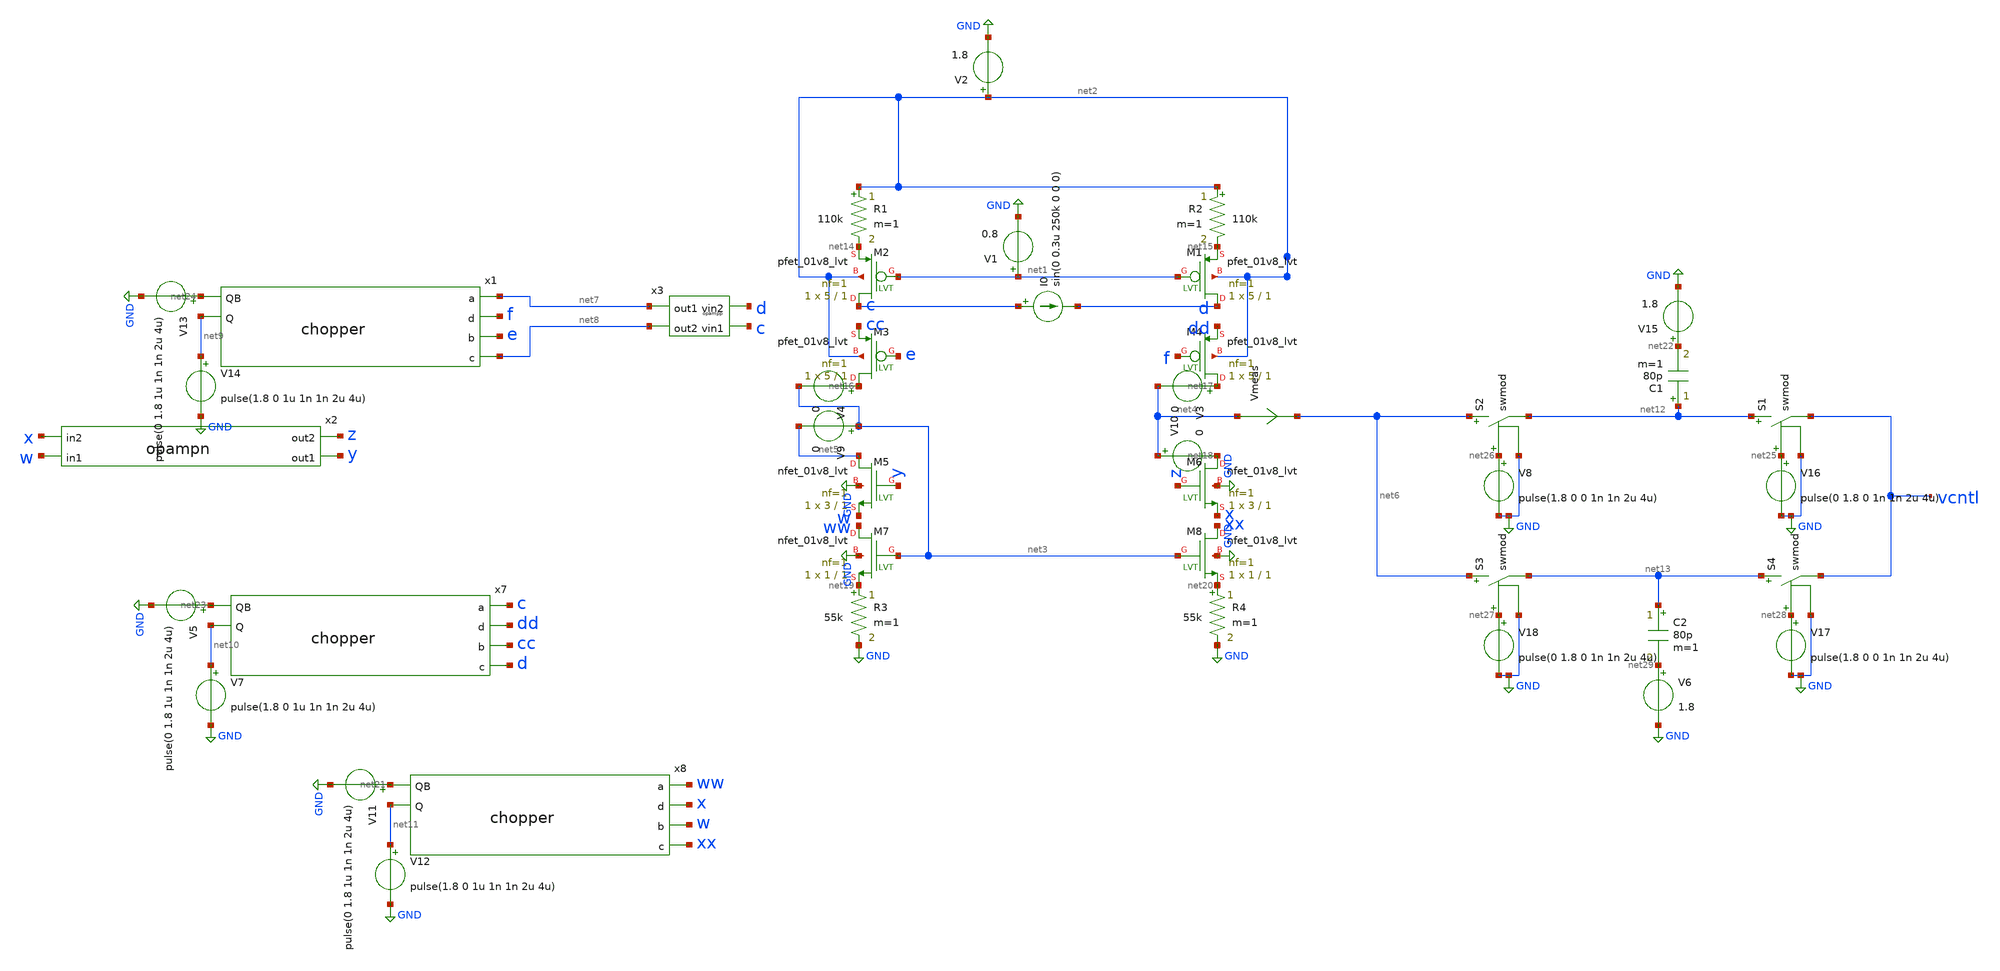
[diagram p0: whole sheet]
** sch_path: currentbuffer.sch
**.subckt currentbuffer
XM2 c net1 net14 net2 sky130_fd_pr__pfet_01v8_lvt L=1 W=5 nf=1 ad='int((nf+1)/2) * W/nf * 0.29' as='int((nf+2)/2) * W/nf * 0.29'
+ pd='2*int((nf+1)/2) * (W/nf + 0.29)' ps='2*int((nf+2)/2) * (W/nf + 0.29)' nrd='0.29 / W' nrs='0.29 / W'
+ sa=0 sb=0 sd=0 mult=1 m=1
R1 net2 net14 110k m=1
XM1 d net1 net15 net2 sky130_fd_pr__pfet_01v8_lvt L=1 W=5 nf=1 ad='int((nf+1)/2) * W/nf * 0.29' as='int((nf+2)/2) * W/nf * 0.29'
+ pd='2*int((nf+1)/2) * (W/nf + 0.29)' ps='2*int((nf+2)/2) * (W/nf + 0.29)' nrd='0.29 / W' nrs='0.29 / W'
+ sa=0 sb=0 sd=0 mult=1 m=1
R2 net2 net15 110k m=1
V1 net1 GND 0.8
XM3 net16 e cc net2 sky130_fd_pr__pfet_01v8_lvt L=1 W=5 nf=1 ad='int((nf+1)/2) * W/nf * 0.29' as='int((nf+2)/2) * W/nf * 0.29'
+ pd='2*int((nf+1)/2) * (W/nf + 0.29)' ps='2*int((nf+2)/2) * (W/nf + 0.29)' nrd='0.29 / W' nrs='0.29 / W'
+ sa=0 sb=0 sd=0 mult=1 m=1
XM4 net17 f dd net2 sky130_fd_pr__pfet_01v8_lvt L=1 W=5 nf=1 ad='int((nf+1)/2) * W/nf * 0.29' as='int((nf+2)/2) * W/nf * 0.29'
+ pd='2*int((nf+1)/2) * (W/nf + 0.29)' ps='2*int((nf+2)/2) * (W/nf + 0.29)' nrd='0.29 / W' nrs='0.29 / W'
+ sa=0 sb=0 sd=0 mult=1 m=1
XM5 net5 y w GND sky130_fd_pr__nfet_01v8_lvt L=1 W=3 nf=1 ad='int((nf+1)/2) * W/nf * 0.29' as='int((nf+2)/2) * W/nf * 0.29'
+ pd='2*int((nf+1)/2) * (W/nf + 0.29)' ps='2*int((nf+2)/2) * (W/nf + 0.29)' nrd='0.29 / W' nrs='0.29 / W'
+ sa=0 sb=0 sd=0 mult=1 m=1
XM6 net18 z x GND sky130_fd_pr__nfet_01v8_lvt L=1 W=3 nf=1 ad='int((nf+1)/2) * W/nf * 0.29' as='int((nf+2)/2) * W/nf * 0.29'
+ pd='2*int((nf+1)/2) * (W/nf + 0.29)' ps='2*int((nf+2)/2) * (W/nf + 0.29)' nrd='0.29 / W' nrs='0.29 / W'
+ sa=0 sb=0 sd=0 mult=1 m=1
XM7 ww net3 net19 GND sky130_fd_pr__nfet_01v8_lvt L=1 W=1 nf=1 ad='int((nf+1)/2) * W/nf * 0.29' as='int((nf+2)/2) * W/nf * 0.29'
+ pd='2*int((nf+1)/2) * (W/nf + 0.29)' ps='2*int((nf+2)/2) * (W/nf + 0.29)' nrd='0.29 / W' nrs='0.29 / W'
+ sa=0 sb=0 sd=0 mult=1 m=1
XM8 xx net3 net20 GND sky130_fd_pr__nfet_01v8_lvt L=1 W=1 nf=1 ad='int((nf+1)/2) * W/nf * 0.29' as='int((nf+2)/2) * W/nf * 0.29'
+ pd='2*int((nf+1)/2) * (W/nf + 0.29)' ps='2*int((nf+2)/2) * (W/nf + 0.29)' nrd='0.29 / W' nrs='0.29 / W'
+ sa=0 sb=0 sd=0 mult=1 m=1
R3 net19 GND 55k m=1
R4 net20 GND 55k m=1
V2 net2 GND 1.8
V9 net3 net5 0
V10 net4 net18 0
V3 net17 net4 0
V4 net16 net3 0
V11 net21 GND pulse(0 1.8 1u 1n 1n 2u 4u)
V12 net11 GND pulse(1.8 0 1u 1n 1n 2u 4u)
C1 net12 net22 80p m=1
V15 net22 GND 1.8
V5 net23 GND pulse(0 1.8 1u 1n 1n 2u 4u)
V7 net10 GND pulse(1.8 0 1u 1n 1n 2u 4u)
V14 net9 GND pulse(1.8 0 1u 1n 1n 2u 4u)
V13 net24 GND pulse(0 1.8 1u 1n 1n 2u 4u)
x3 d c net7 net8 opampp
x2 z y x w opampn
I0 c d sin(0 0.3u 250k 0 0 0)
Vmeas net4 net6 0
.save i(vmeas)
x1 net7 net24 net9 f e net8 chopper
x7 c net23 net10 dd cc d chopper
x8 ww net21 net11 x w xx chopper
S1 net12 vcntl net25 GND swmod
S2 net6 net12 net26 GND swmod
S3 net6 net13 net27 GND swmod
S4 net13 vcntl net28 GND swmod
C2 net13 net29 80p m=1
V6 net29 GND 1.8
V8 net26 GND pulse(1.8 0 0 1n 1n 2u 4u)
V16 net25 GND pulse(0 1.8 0 1n 1n 2u 4u)
V17 net28 GND pulse(1.8 0 0 1n 1n 2u 4u)
V18 net27 GND pulse(0 1.8 0 1n 1n 2u 4u)
**** begin user architecture code



.tran 1n 10u
.control
*foreach x -90 -45 0 45 90
*alter @I0[sin] [0 0.3u 250k 0 0 $x]
save all
run
meas tran average avg i(vmeas) from=2u to=8u
*end
.endc





.param mc_mm_switch=0
.param mc_pr_switch=0

.include ~/open_pdks/sky130/sky130A/libs.tech/ngspice/corners/tt/nonfet.spice
.include ~/open_pdks/sky130/sky130A/libs.ref/sky130_fd_pr/spice/sky130_fd_pr__pfet_01v8__tt.corner.spice
.inclued ~/open_pdks/sky130/sky130A/libs.ref/sky130_fd_pr/spice/sky130_fd_pr__nfet_01v8__tt.corner.spice

*mismatch parameters
.include ~/open_pdks/sky130/sky130A/libs.ref/sky130_fd_pr/spice/sky130_fd_pr__pfet_01v8__mismatch.corner.spice
.include ~/open_pdks/sky130/sky130A/libs.ref/sky130_fd_pr/spice/sky130_fd_pr__nfet_01v8__mismatch.corner.spice

*model
.include ~/open_pdks/sky130/sky130A/libs.tech/ngspice/all.spice

*mosfet
.include ~/open_pdks/sky130/sky130A/libs.ref/sky130_fd_pr/spice/sky130_fd_pr__pfet_01v8_lvt__tt.corner.spice
.inclued ~/open_pdks/sky130/sky130A/libs.ref/sky130_fd_pr/spice/sky130_fd_pr__nfet_01v8_lvt__tt.corner.spice

*mismatch parameters
.include ~/open_pdks/sky130/sky130A/libs.ref/sky130_fd_pr/spice/sky130_fd_pr__pfet_01v8_lvt__mismatch.corner.spice
.include ~/open_pdks/sky130/sky130A/libs.ref/sky130_fd_pr/spice/sky130_fd_pr__nfet_01v8_lvt__mismatch.corner.spice
.MODEL swmod SW(VT=0.9 VH=0 RON=1 ROFF=1000000000000000)


**** end user architecture code
**.ends

* expanding   symbol:  /home/cegrahul/Downloads/opampp.sym # of pins=4
** sym_path: opampp.sym
** sch_path: opampp.sch
.subckt opampp vin2 vin1 out1 out2
*.opin out1
*.opin out2
*.ipin vin1
*.ipin vin2
XM1 out1 net1 GND GND sky130_fd_pr__nfet_01v8_lvt L=4 W=1 nf=1 ad='int((nf+1)/2) * W/nf * 0.29' as='int((nf+2)/2) * W/nf * 0.29'
+ pd='2*int((nf+1)/2) * (W/nf + 0.29)' ps='2*int((nf+2)/2) * (W/nf + 0.29)' nrd='0.29 / W' nrs='0.29 / W'
+ sa=0 sb=0 sd=0 mult=1 m=1
XM2 out1 vin1 net2 net3 sky130_fd_pr__pfet_01v8_lvt L=1 W=3 nf=1 ad='int((nf+1)/2) * W/nf * 0.29' as='int((nf+2)/2) * W/nf * 0.29'
+ pd='2*int((nf+1)/2) * (W/nf + 0.29)' ps='2*int((nf+2)/2) * (W/nf + 0.29)' nrd='0.29 / W' nrs='0.29 / W'
+ sa=0 sb=0 sd=0 mult=1 m=1
XM3 out2 vin2 net2 net3 sky130_fd_pr__pfet_01v8_lvt L=1 W=3 nf=1 ad='int((nf+1)/2) * W/nf * 0.29' as='int((nf+2)/2) * W/nf * 0.29'
+ pd='2*int((nf+1)/2) * (W/nf + 0.29)' ps='2*int((nf+2)/2) * (W/nf + 0.29)' nrd='0.29 / W' nrs='0.29 / W'
+ sa=0 sb=0 sd=0 mult=1 m=1
XM4 out2 net1 GND GND sky130_fd_pr__nfet_01v8_lvt L=4 W=1 nf=1 ad='int((nf+1)/2) * W/nf * 0.29' as='int((nf+2)/2) * W/nf * 0.29'
+ pd='2*int((nf+1)/2) * (W/nf + 0.29)' ps='2*int((nf+2)/2) * (W/nf + 0.29)' nrd='0.29 / W' nrs='0.29 / W'
+ sa=0 sb=0 sd=0 mult=1 m=1
V1 net3 GND 1.8
V3 net1 GND 0.561
R1 net3 net2 165k m=1
.ends


* expanding   symbol:  /home/cegrahul/Downloads/opampn.sym # of pins=4
** sym_path: opampn.sym
** sch_path: opampn.sch
.subckt opampn out2 out1 in2 in1
*.ipin in1
*.ipin in2
*.opin out1
*.opin out2
XM1 out1 in1 net1 GND sky130_fd_pr__nfet_01v8_lvt L=2 W=1 nf=1 ad='int((nf+1)/2) * W/nf * 0.29' as='int((nf+2)/2) * W/nf * 0.29'
+ pd='2*int((nf+1)/2) * (W/nf + 0.29)' ps='2*int((nf+2)/2) * (W/nf + 0.29)' nrd='0.29 / W' nrs='0.29 / W'
+ sa=0 sb=0 sd=0 mult=1 m=1
XM2 out2 in2 net1 GND sky130_fd_pr__nfet_01v8_lvt L=2 W=1 nf=1 ad='int((nf+1)/2) * W/nf * 0.29' as='int((nf+2)/2) * W/nf * 0.29'
+ pd='2*int((nf+1)/2) * (W/nf + 0.29)' ps='2*int((nf+2)/2) * (W/nf + 0.29)' nrd='0.29 / W' nrs='0.29 / W'
+ sa=0 sb=0 sd=0 mult=1 m=1
XM3 out1 net5 net2 net4 sky130_fd_pr__pfet_01v8_lvt L=2 W=5 nf=1 ad='int((nf+1)/2) * W/nf * 0.29' as='int((nf+2)/2) * W/nf * 0.29'
+ pd='2*int((nf+1)/2) * (W/nf + 0.29)' ps='2*int((nf+2)/2) * (W/nf + 0.29)' nrd='0.29 / W' nrs='0.29 / W'
+ sa=0 sb=0 sd=0 mult=1 m=1
XM4 out2 net5 net3 net4 sky130_fd_pr__pfet_01v8_lvt L=2 W=5 nf=1 ad='int((nf+1)/2) * W/nf * 0.29' as='int((nf+2)/2) * W/nf * 0.29'
+ pd='2*int((nf+1)/2) * (W/nf + 0.29)' ps='2*int((nf+2)/2) * (W/nf + 0.29)' nrd='0.29 / W' nrs='0.29 / W'
+ sa=0 sb=0 sd=0 mult=1 m=1
R1 net1 GND 165k m=1
R2 net4 net2 330k m=1
R3 net4 net3 330k m=1
V1 net4 GND 1.8
V2 net5 GND 1.08
.ends


* expanding   symbol:  /home/cegrahul/Desktop/SSCS/chopper.sym # of pins=6
** sym_path: chopper.sym
** sch_path: chopper.sch
.subckt chopper a QB Q d b c
*.ipin QB
*.ipin Q
*.opin a
*.opin d
*.opin b
*.opin c
XM1 a Q b GND sky130_fd_pr__nfet_01v8 L=0.15 W=1 nf=1 ad='int((nf+1)/2) * W/nf * 0.29' as='int((nf+2)/2) * W/nf * 0.29'
+ pd='2*int((nf+1)/2) * (W/nf + 0.29)' ps='2*int((nf+2)/2) * (W/nf + 0.29)' nrd='0.29 / W' nrs='0.29 / W'
+ sa=0 sb=0 sd=0 mult=1 m=1
XM2 b QB a VDD sky130_fd_pr__pfet_01v8 L=0.15 W=1 nf=1 ad='int((nf+1)/2) * W/nf * 0.29' as='int((nf+2)/2) * W/nf * 0.29'
+ pd='2*int((nf+1)/2) * (W/nf + 0.29)' ps='2*int((nf+2)/2) * (W/nf + 0.29)' nrd='0.29 / W' nrs='0.29 / W'
+ sa=0 sb=0 sd=0 mult=2 m=2
XM3 c Q d GND sky130_fd_pr__nfet_01v8 L=0.15 W=1 nf=1 ad='int((nf+1)/2) * W/nf * 0.29' as='int((nf+2)/2) * W/nf * 0.29'
+ pd='2*int((nf+1)/2) * (W/nf + 0.29)' ps='2*int((nf+2)/2) * (W/nf + 0.29)' nrd='0.29 / W' nrs='0.29 / W'
+ sa=0 sb=0 sd=0 mult=1 m=1
XM4 d QB c VDD sky130_fd_pr__pfet_01v8 L=0.15 W=1 nf=1 ad='int((nf+1)/2) * W/nf * 0.29' as='int((nf+2)/2) * W/nf * 0.29'
+ pd='2*int((nf+1)/2) * (W/nf + 0.29)' ps='2*int((nf+2)/2) * (W/nf + 0.29)' nrd='0.29 / W' nrs='0.29 / W'
+ sa=0 sb=0 sd=0 mult=2 m=2
XM5 a QB d GND sky130_fd_pr__nfet_01v8 L=0.15 W=1 nf=1 ad='int((nf+1)/2) * W/nf * 0.29' as='int((nf+2)/2) * W/nf * 0.29'
+ pd='2*int((nf+1)/2) * (W/nf + 0.29)' ps='2*int((nf+2)/2) * (W/nf + 0.29)' nrd='0.29 / W' nrs='0.29 / W'
+ sa=0 sb=0 sd=0 mult=1 m=1
XM6 d Q a VDD sky130_fd_pr__pfet_01v8 L=0.15 W=1 nf=1 ad='int((nf+1)/2) * W/nf * 0.29' as='int((nf+2)/2) * W/nf * 0.29'
+ pd='2*int((nf+1)/2) * (W/nf + 0.29)' ps='2*int((nf+2)/2) * (W/nf + 0.29)' nrd='0.29 / W' nrs='0.29 / W'
+ sa=0 sb=0 sd=0 mult=2 m=2
XM7 c QB b GND sky130_fd_pr__nfet_01v8 L=0.15 W=1 nf=1 ad='int((nf+1)/2) * W/nf * 0.29' as='int((nf+2)/2) * W/nf * 0.29'
+ pd='2*int((nf+1)/2) * (W/nf + 0.29)' ps='2*int((nf+2)/2) * (W/nf + 0.29)' nrd='0.29 / W' nrs='0.29 / W'
+ sa=0 sb=0 sd=0 mult=1 m=1
XM8 b Q c VDD sky130_fd_pr__pfet_01v8 L=0.15 W=1 nf=1 ad='int((nf+1)/2) * W/nf * 0.29' as='int((nf+2)/2) * W/nf * 0.29'
+ pd='2*int((nf+1)/2) * (W/nf + 0.29)' ps='2*int((nf+2)/2) * (W/nf + 0.29)' nrd='0.29 / W' nrs='0.29 / W'
+ sa=0 sb=0 sd=0 mult=2 m=2
.ends

.GLOBAL GND
.end
